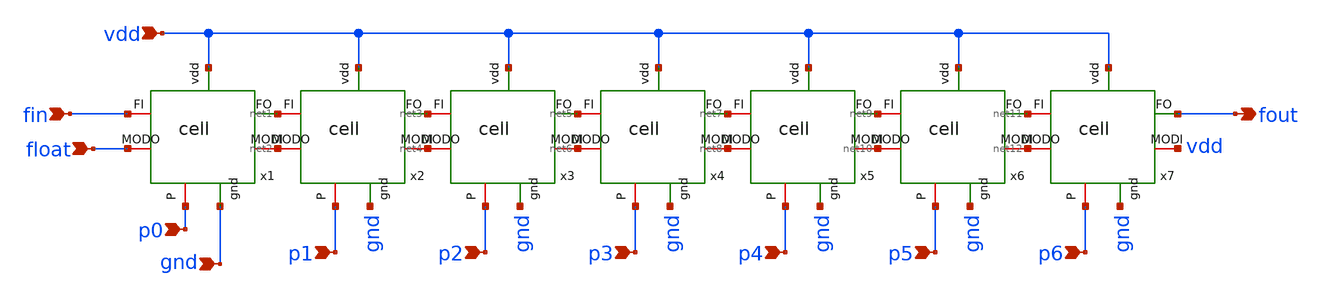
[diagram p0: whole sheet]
** sch_path: pll/dividers_lib/divider_design_trials/divider_2by3stages/divider.sch
**.subckt divider vdd gnd fout p0 p4 p5 p6 p3 p2 p1 fin float
*.ipin vdd
*.ipin gnd
*.opin fout
*.ipin p0
*.ipin p4
*.ipin p5
*.ipin p6
*.ipin p3
*.ipin p2
*.ipin p1
*.ipin fin
*.ipin float
x1 vdd net1 net2 p0 gnd fin float cell
x2 vdd net3 net4 p1 gnd net1 net2 cell
x3 vdd net5 net6 p2 gnd net3 net4 cell
x4 vdd net7 net8 p3 gnd net5 net6 cell
x5 vdd net9 net10 p4 gnd net7 net8 cell
x6 vdd net11 net12 p5 gnd net9 net10 cell
x7 vdd fout vdd p6 gnd net11 net12 cell
**.ends
.end
